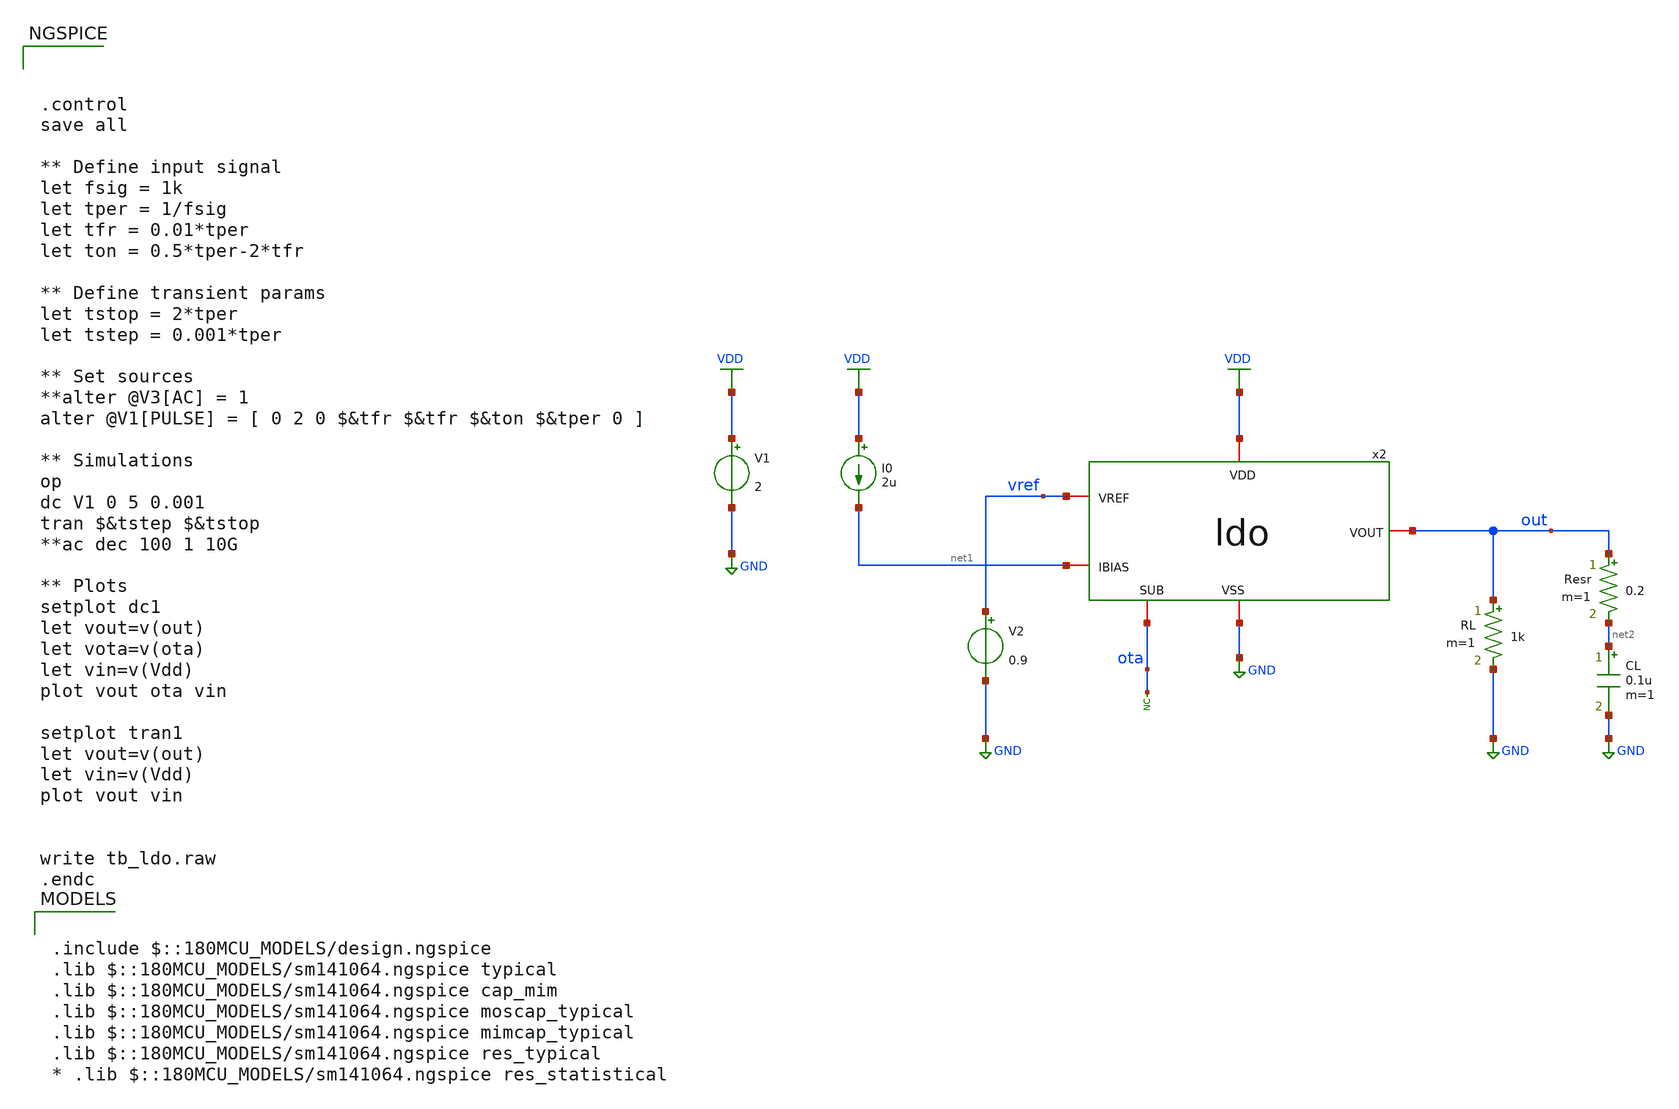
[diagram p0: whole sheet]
** sch_path: designs/libs/tb_ldo/tb_ldo/tb_ldo.sch
**.subckt tb_ldo
* noconn ota
RL out GND 1k m=1
V1 VDD GND 2
V2 vref GND 0.9
I0 VDD net1 2u
CL net2 GND 0.1u m=1
Resr out net2 0.2 m=1
x2 VDD vref out net1 ota GND ldo
**** begin user architecture code

.include $::180MCU_MODELS/design.ngspice
.lib $::180MCU_MODELS/sm141064.ngspice typical
.lib $::180MCU_MODELS/sm141064.ngspice cap_mim
.lib $::180MCU_MODELS/sm141064.ngspice moscap_typical
.lib $::180MCU_MODELS/sm141064.ngspice mimcap_typical
.lib $::180MCU_MODELS/sm141064.ngspice res_typical
* .lib $::180MCU_MODELS/sm141064.ngspice res_statistical




.control
save all

** Define input signal
let fsig = 1k
let tper = 1/fsig
let tfr = 0.01*tper
let ton = 0.5*tper-2*tfr

** Define transient params
let tstop = 2*tper
let tstep = 0.001*tper

** Set sources
**alter @V3[AC] = 1
alter @V1[PULSE] = [ 0 2 0 $&tfr $&tfr $&ton $&tper 0 ]

** Simulations
op
dc V1 0 5 0.001
tran $&tstep $&tstop
**ac dec 100 1 10G

** Plots
setplot dc1
let vout=v(out)
let vota=v(ota)
let vin=v(Vdd)
plot vout ota vin

setplot tran1
let vout=v(out)
let vin=v(Vdd)
plot vout vin


write tb_ldo.raw
.endc


**** end user architecture code
**.ends
.GLOBAL GND
.GLOBAL VDD
.end
